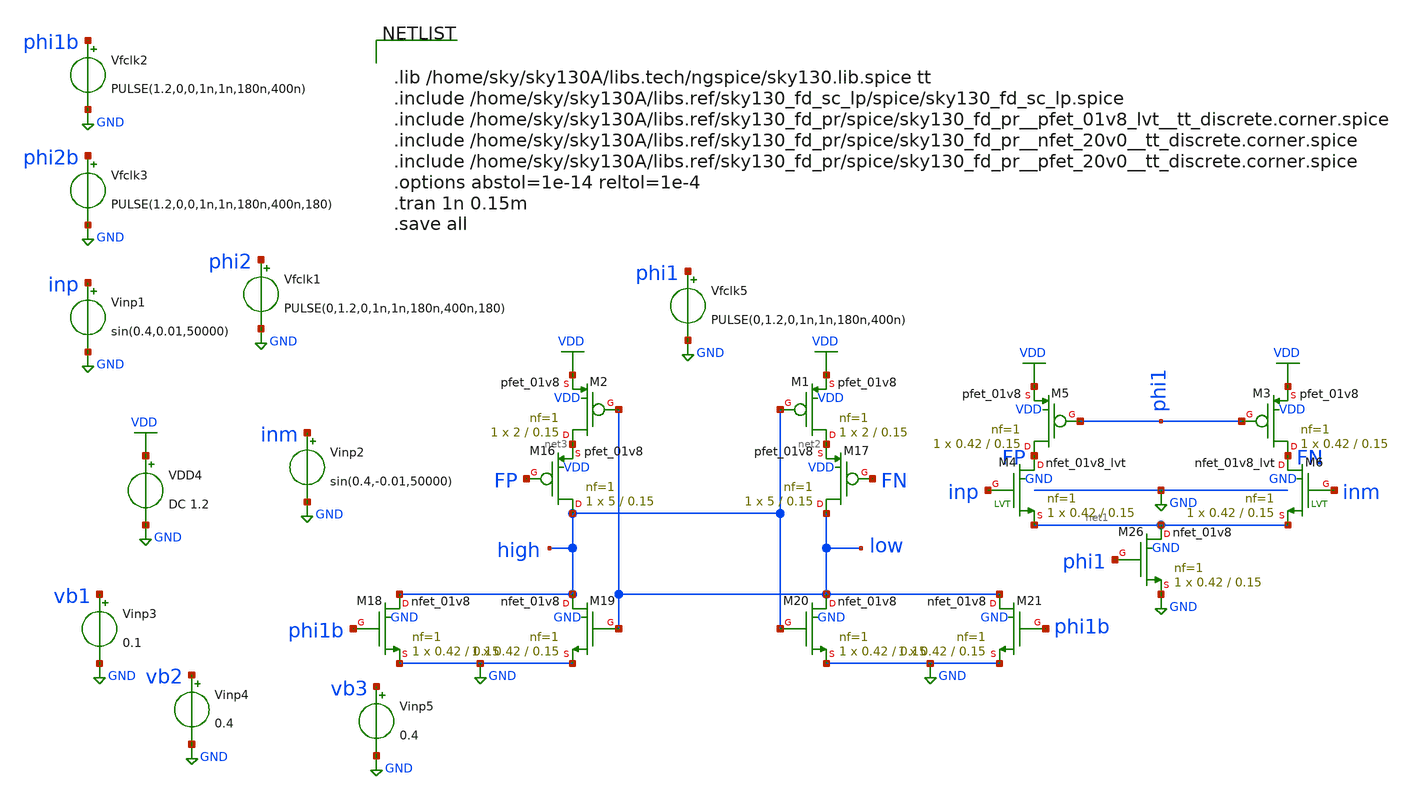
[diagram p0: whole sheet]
** sch_path: xschem/comparator_with_AZ/comparator_AZ_tb.sch
**.subckt comparator_AZ_tb
VDD4 VDD GND DC 1.2
Vfclk5 phi1 GND PULSE(0,1.2,0,1n,1n,180n,400n)
XM1 net2 high VDD VDD sky130_fd_pr__pfet_01v8 L=0.15 W=2 nf=1 ad='int((nf+1)/2) * W/nf * 0.29' as='int((nf+2)/2) * W/nf * 0.29'
+ pd='2*int((nf+1)/2) * (W/nf + 0.29)' ps='2*int((nf+2)/2) * (W/nf + 0.29)' nrd='0.29 / W' nrs='0.29 / W'
+ sa=0 sb=0 sd=0 mult=1 m=1
XM2 net3 low VDD VDD sky130_fd_pr__pfet_01v8 L=0.15 W=2 nf=1 ad='int((nf+1)/2) * W/nf * 0.29' as='int((nf+2)/2) * W/nf * 0.29'
+ pd='2*int((nf+1)/2) * (W/nf + 0.29)' ps='2*int((nf+2)/2) * (W/nf + 0.29)' nrd='0.29 / W' nrs='0.29 / W'
+ sa=0 sb=0 sd=0 mult=1 m=1
XM16 high FP net3 VDD sky130_fd_pr__pfet_01v8 L=0.15 W=5 nf=1 ad='int((nf+1)/2) * W/nf * 0.29' as='int((nf+2)/2) * W/nf * 0.29'
+ pd='2*int((nf+1)/2) * (W/nf + 0.29)' ps='2*int((nf+2)/2) * (W/nf + 0.29)' nrd='0.29 / W' nrs='0.29 / W'
+ sa=0 sb=0 sd=0 mult=1 m=1
XM17 low FN net2 VDD sky130_fd_pr__pfet_01v8 L=0.15 W=5 nf=1 ad='int((nf+1)/2) * W/nf * 0.29' as='int((nf+2)/2) * W/nf * 0.29'
+ pd='2*int((nf+1)/2) * (W/nf + 0.29)' ps='2*int((nf+2)/2) * (W/nf + 0.29)' nrd='0.29 / W' nrs='0.29 / W'
+ sa=0 sb=0 sd=0 mult=1 m=1
XM18 high phi1b GND GND sky130_fd_pr__nfet_01v8 L=0.15 W=0.42 nf=1 ad='int((nf+1)/2) * W/nf * 0.29' as='int((nf+2)/2) * W/nf * 0.29'
+ pd='2*int((nf+1)/2) * (W/nf + 0.29)' ps='2*int((nf+2)/2) * (W/nf + 0.29)' nrd='0.29 / W' nrs='0.29 / W'
+ sa=0 sb=0 sd=0 mult=1 m=1
XM19 high low GND GND sky130_fd_pr__nfet_01v8 L=0.15 W=0.42 nf=1 ad='int((nf+1)/2) * W/nf * 0.29' as='int((nf+2)/2) * W/nf * 0.29'
+ pd='2*int((nf+1)/2) * (W/nf + 0.29)' ps='2*int((nf+2)/2) * (W/nf + 0.29)' nrd='0.29 / W' nrs='0.29 / W'
+ sa=0 sb=0 sd=0 mult=1 m=1
XM20 low high GND GND sky130_fd_pr__nfet_01v8 L=0.15 W=0.42 nf=1 ad='int((nf+1)/2) * W/nf * 0.29' as='int((nf+2)/2) * W/nf * 0.29'
+ pd='2*int((nf+1)/2) * (W/nf + 0.29)' ps='2*int((nf+2)/2) * (W/nf + 0.29)' nrd='0.29 / W' nrs='0.29 / W'
+ sa=0 sb=0 sd=0 mult=1 m=1
XM21 low phi1b GND GND sky130_fd_pr__nfet_01v8 L=0.15 W=0.42 nf=1 ad='int((nf+1)/2) * W/nf * 0.29' as='int((nf+2)/2) * W/nf * 0.29'
+ pd='2*int((nf+1)/2) * (W/nf + 0.29)' ps='2*int((nf+2)/2) * (W/nf + 0.29)' nrd='0.29 / W' nrs='0.29 / W'
+ sa=0 sb=0 sd=0 mult=1 m=1
XM26 net1 phi1 GND GND sky130_fd_pr__nfet_01v8 L=0.15 W=0.42 nf=1 ad='int((nf+1)/2) * W/nf * 0.29' as='int((nf+2)/2) * W/nf * 0.29'
+ pd='2*int((nf+1)/2) * (W/nf + 0.29)' ps='2*int((nf+2)/2) * (W/nf + 0.29)' nrd='0.29 / W' nrs='0.29 / W'
+ sa=0 sb=0 sd=0 mult=1 m=1
Vinp1 inp GND sin(0.4,0.01,50000)
Vinp2 inm GND sin(0.4,-0.01,50000)
Vfclk1 phi2 GND PULSE(0,1.2,0,1n,1n,180n,400n,180)
Vfclk2 phi1b GND PULSE(1.2,0,0,1n,1n,180n,400n)
Vfclk3 phi2b GND PULSE(1.2,0,0,1n,1n,180n,400n,180)
XM3 FN phi1 VDD VDD sky130_fd_pr__pfet_01v8 L=0.15 W=0.42 nf=1 ad='int((nf+1)/2) * W/nf * 0.29' as='int((nf+2)/2) * W/nf * 0.29'
+ pd='2*int((nf+1)/2) * (W/nf + 0.29)' ps='2*int((nf+2)/2) * (W/nf + 0.29)' nrd='0.29 / W' nrs='0.29 / W'
+ sa=0 sb=0 sd=0 mult=1 m=1
XM5 FP phi1 VDD VDD sky130_fd_pr__pfet_01v8 L=0.15 W=0.42 nf=1 ad='int((nf+1)/2) * W/nf * 0.29' as='int((nf+2)/2) * W/nf * 0.29'
+ pd='2*int((nf+1)/2) * (W/nf + 0.29)' ps='2*int((nf+2)/2) * (W/nf + 0.29)' nrd='0.29 / W' nrs='0.29 / W'
+ sa=0 sb=0 sd=0 mult=1 m=1
Vinp3 vb1 GND 0.1
Vinp4 vb2 GND 0.4
Vinp5 vb3 GND 0.4
XM4 FP inp net1 GND sky130_fd_pr__nfet_01v8_lvt L=0.15 W=0.42 nf=1 ad='int((nf+1)/2) * W/nf * 0.29' as='int((nf+2)/2) * W/nf * 0.29'
+ pd='2*int((nf+1)/2) * (W/nf + 0.29)' ps='2*int((nf+2)/2) * (W/nf + 0.29)' nrd='0.29 / W' nrs='0.29 / W'
+ sa=0 sb=0 sd=0 mult=1 m=1
XM6 FN inm net1 GND sky130_fd_pr__nfet_01v8_lvt L=0.15 W=0.42 nf=1 ad='int((nf+1)/2) * W/nf * 0.29' as='int((nf+2)/2) * W/nf * 0.29'
+ pd='2*int((nf+1)/2) * (W/nf + 0.29)' ps='2*int((nf+2)/2) * (W/nf + 0.29)' nrd='0.29 / W' nrs='0.29 / W'
+ sa=0 sb=0 sd=0 mult=1 m=1
**** begin user architecture code


.lib /home/sky/sky130A/libs.tech/ngspice/sky130.lib.spice tt
.include /home/sky/sky130A/libs.ref/sky130_fd_sc_lp/spice/sky130_fd_sc_lp.spice
.include /home/sky/sky130A/libs.ref/sky130_fd_pr/spice/sky130_fd_pr__pfet_01v8_lvt__tt_discrete.corner.spice
.include /home/sky/sky130A/libs.ref/sky130_fd_pr/spice/sky130_fd_pr__nfet_20v0__tt_discrete.corner.spice
.include /home/sky/sky130A/libs.ref/sky130_fd_pr/spice/sky130_fd_pr__pfet_20v0__tt_discrete.corner.spice
.options abstol=1e-14 reltol=1e-4
.tran 1n 0.15m
.save all


**** end user architecture code
**.ends
.GLOBAL GND
.GLOBAL VDD
.end
